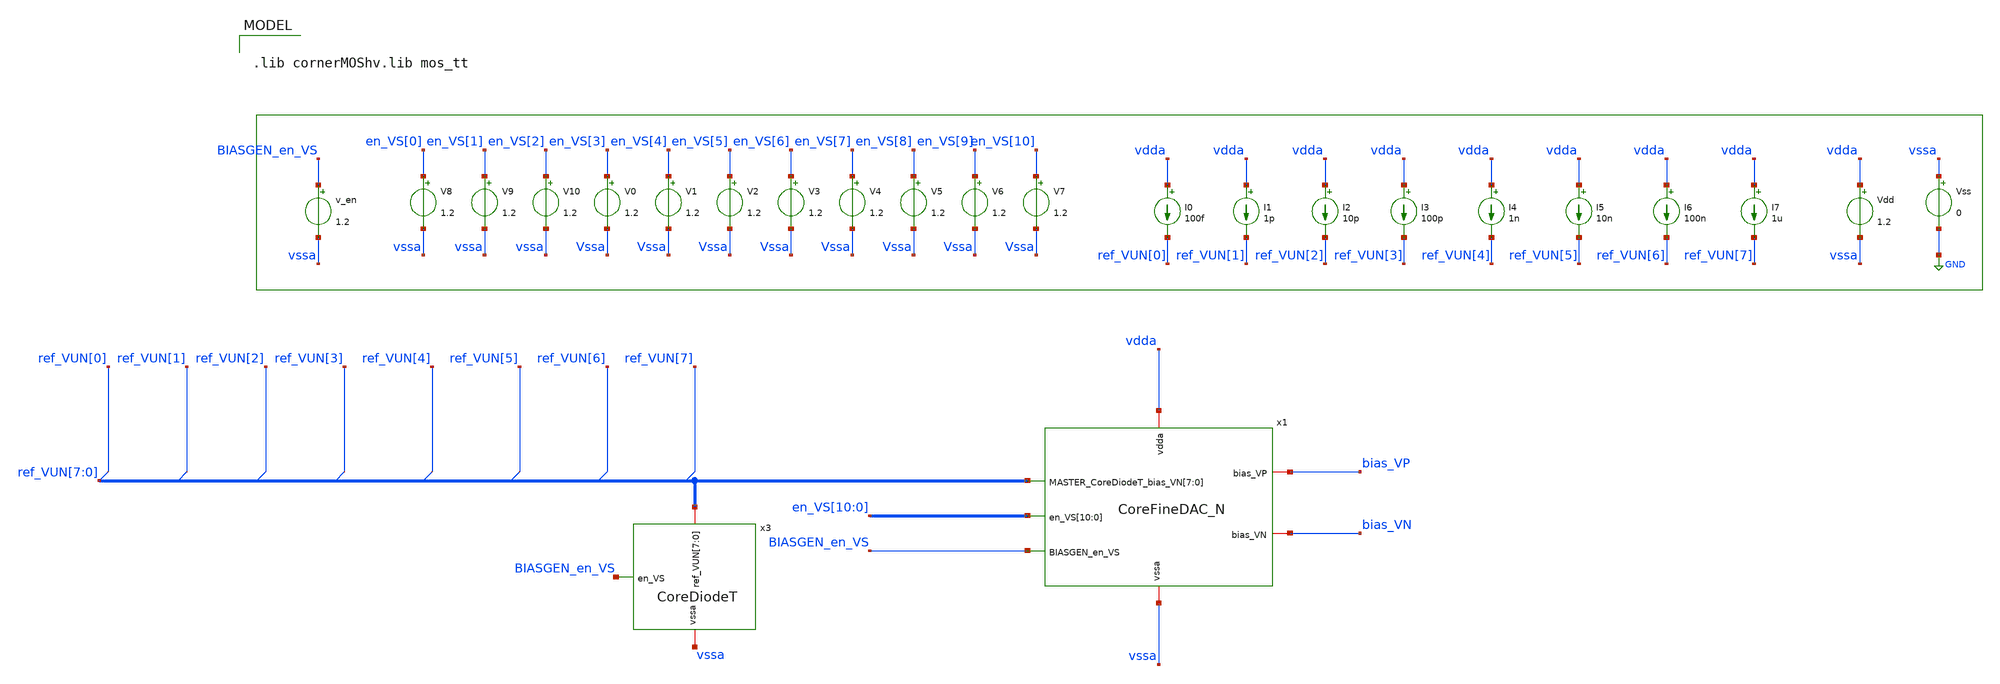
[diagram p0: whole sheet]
** sch_path: test_bench/CoreFineDAC_N_dc_tb.sch
**.subckt CoreFineDAC_N_dc_tb
Vdd vdda vssa 1.2
V0 en_VS[3] Vssa 1.2
Vss vssa GND 0
V1 en_VS[4] Vssa 1.2
V2 en_VS[5] Vssa 1.2
V3 en_VS[6] Vssa 1.2
V4 en_VS[7] Vssa 1.2
V5 en_VS[8] Vssa 1.2
V6 en_VS[9] Vssa 1.2
V7 en_VS[10] Vssa 1.2
V8 en_VS[0] vssa 1.2
V9 en_VS[1] vssa 1.2
V10 en_VS[2] vssa 1.2
I0 vdda ref_VUN[0] 100f
I1 vdda ref_VUN[1] 1p
I2 vdda ref_VUN[2] 10p
I3 vdda ref_VUN[3] 100p
I4 vdda ref_VUN[4] 1n
I6 vdda ref_VUN[6] 100n
I5 vdda ref_VUN[5] 10n
I7 vdda ref_VUN[7] 1u
v_en BIASGEN_en_VS vssa 1.2
x1 en_VS[10] en_VS[9] en_VS[8] en_VS[7] en_VS[6] en_VS[5] en_VS[4] en_VS[3] en_VS[2] en_VS[1]
+ en_VS[0] vssa vdda bias_VP bias_VN ref_VUN[7] ref_VUN[6] ref_VUN[5] ref_VUN[4] ref_VUN[3] ref_VUN[2]
+ ref_VUN[1] ref_VUN[0] BIASGEN_en_VS CoreFineDAC_N
x3 ref_VUN[7] ref_VUN[6] ref_VUN[5] ref_VUN[4] ref_VUN[3] ref_VUN[2] ref_VUN[1] ref_VUN[0] vssa
+ BIASGEN_en_VS CoreDiodeT
**** begin user architecture code

.lib cornerMOShv.lib mos_tt



.param temp=27

.options abstol=5e-15
.options gmin=5e-15
.options gmindc=5e-15
.control
let V_drain_ISINK_vect = vector(16)
let initial_range = 1
let code_range = initial_range
let max_range = initial_range +1
let digitalCommand = vector(16)
let out_UP = vector(16)
let V_out_UP = vector(16)
while code_range < max_range
    * Set the 3 bits
    alter V8 = 1.2*(code_range % 2)
    alter V9 = 1.2*(floor(code_range/2) % 2)
    alter V10 = 1.2*(floor(code_range/4) % 2)
    let min = 240
    let max = 256
    let code = min
    while code < max
      save all
      * Set the 8 bits
      alter V0 = 1.2*(code % 2)
      alter V1 = 1.2*(floor(code/2) % 2)
      alter V2 = 1.2*(floor(code/4) % 2)
      alter V3 = 1.2*(floor(code/8) % 2)
      alter V4 = 1.2*(floor(code/16) % 2)
      alter V5 = 1.2*(floor(code/32) % 2)
      alter V6 = 1.2*(floor(code/64) % 2)
      alter V7 = 1.2*(floor(code/128) % 2)

      op

      let digitalCommand[code-min] = code
      let out_UP[code-min] = I(V.x1.V_out_UP)
      let V_out_UP[code-min] = V(bias_VP)
      let V_drain_ISINK_vect[code-min] = V(x1.V_drain_ISINK)
      * let out_UP[code-min] = I(V.x1.V_Ibias1)
      let code = code + 1
      print code
      * write CoreFineDAC_N_dc_tb/full_op_{$&code_range}.raw
   end
   setplot const
   settype current out_UP
   settype voltage V_out_UP
   settype voltage V_drain_ISINK_vect
   setscale digitalCommand
   plot out_UP
   plot V_out_UP
   plot V_drain_ISINK_vect

   let code_range = code_range + 1
   write  simulations/CoreFineDAC_N_dc_tb/commandRange_{$&initial_range}_{$&max}.raw out_UP V_out_UP
+ V_drain_ISINK_vect
   *write CoreFineDAC_N_dc_tb/commandRange_{$&initial_range}_{$&max}.raw out_UP
end


.endc





**** end user architecture code
**.ends
.GLOBAL GND
.end
